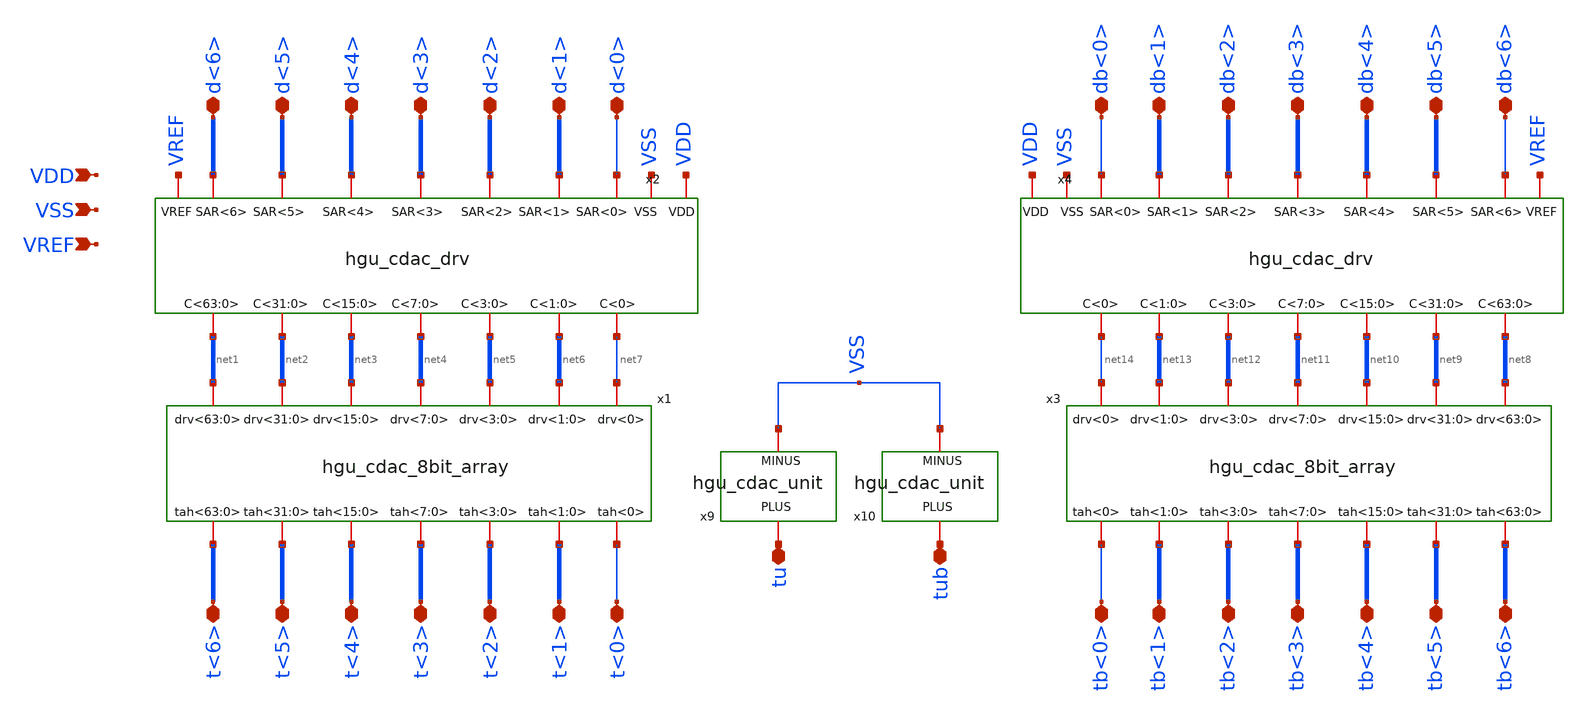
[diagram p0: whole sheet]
** sch_path: hgu/xschem/hgu_cdac_half.sch
**.subckt hgu_cdac_half d<6> d<5> d<4> d<3> d<2> d<1> d<0> db<6> db<5> db<4> db<3> db<2> db<1> db<0>
*+ VSS VREF t<6> t<5> t<4> t<3> t<2> t<1> t<0> tb<6> tb<5> tb<4> tb<3> tb<2> tb<1> tb<0> tu tub VDD
*.iopin d<6>
*.iopin d<5>
*.iopin d<4>
*.iopin d<3>
*.iopin d<2>
*.iopin d<1>
*.iopin d<0>
*.iopin db<6>
*.iopin db<5>
*.iopin db<4>
*.iopin db<3>
*.iopin db<2>
*.iopin db<1>
*.iopin db<0>
*.ipin VSS
*.ipin VREF
*.iopin t<6>
*.iopin t<5>
*.iopin t<4>
*.iopin t<3>
*.iopin t<2>
*.iopin t<1>
*.iopin t<0>
*.iopin tb<6>
*.iopin tb<5>
*.iopin tb<4>
*.iopin tb<3>
*.iopin tb<2>
*.iopin tb<1>
*.iopin tb<0>
*.iopin tu
*.iopin tub
*.ipin VDD
x1 net2 net6 net7 net5 net1 net3 net4 t<6> t<5> t<4> t<3> t<2> t<1> t<0> hgu_cdac_8bit_array
x2 VREF d<4> d<1> d<2> d<3> d<5> d<6> d<0> net5 net4 net3 net2 net7 net6 net1 VSS VDD hgu_cdac_drv
x3 net9 net13 net14 net12 net8 net10 net11 tb<6> tb<5> tb<4> tb<3> tb<2> tb<1> tb<0>
+ hgu_cdac_8bit_array
x4 VREF db<4> db<1> db<2> db<3> db<5> db<6> db<0> net12 net11 net10 net9 net14 net13 net8 VSS VDD
+ hgu_cdac_drv
x9 tu VSS hgu_cdac_unit csize=1
x10 tub VSS hgu_cdac_unit csize=1
**.ends
.end
